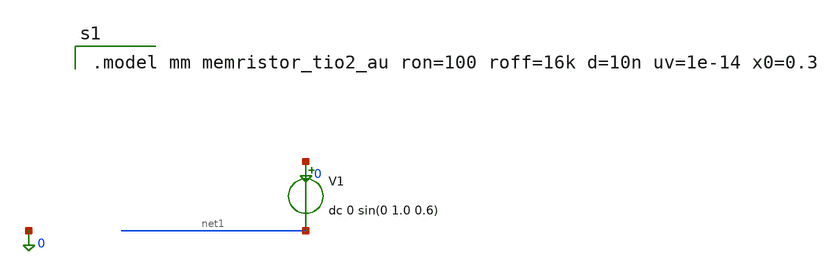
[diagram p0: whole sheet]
** sch_path: libraries/openmemristorpdk_pr/memristor_tio2_au.sch
**.subckt memristor_tio2_au
V1 0 net1 dc 0 sin(0 1.0 0.6)
**** begin user architecture code

.model mm memristor_tio2_au ron=100 roff=16k d=10n uv=1e-14 x0=0.3

**** end user architecture code
**.ends
.end
